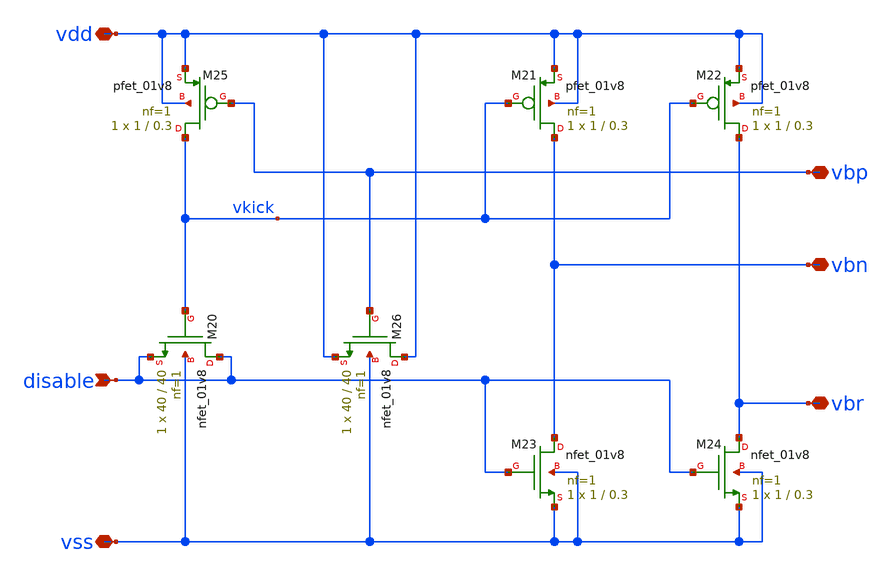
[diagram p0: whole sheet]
** sch_path: playground/ToBiasStartup.sch
**.subckt ToBiasStartup vss vdd vbp vbn vbr disable
*.iopin vss
*.iopin vdd
*.iopin vbp
*.iopin vbn
*.iopin vbr
*.ipin disable
XM24 vbr disable vss vss sky130_fd_pr__nfet_01v8 L=0.3 W=1 nf=1 ad='int((1 + 1)/2) * 1 / 1 * 0.29' as='int((1 + 2)/2) * 1 / 1 * 0.29'
+ pd='2*int((1 + 1)/2) * (1 / 1 + 0.29)' ps='2*int((1 + 2)/2) * (1 / 1 + 0.29)' nrd='0.29 / 1 ' nrs='0.29 / 1 '
+ sa=0 sb=0 sd=0 mult=1 m=1
XM22 vbr vkick vdd vdd sky130_fd_pr__pfet_01v8 L=0.3 W=1 nf=1 ad='int((nf+1)/2) * W/nf * 0.29' as='int((nf+2)/2) * W/nf * 0.29'
+ pd='2*int((nf+1)/2) * (W/nf + 0.29)' ps='2*int((nf+2)/2) * (W/nf + 0.29)' nrd='0.29 / W' nrs='0.29 / W'
+ sa=0 sb=0 sd=0 mult=1 m=1
XM25 vkick vbp vdd vdd sky130_fd_pr__pfet_01v8 L=0.3 W=1 nf=1 ad='int((nf+1)/2) * W/nf * 0.29' as='int((nf+2)/2) * W/nf * 0.29'
+ pd='2*int((nf+1)/2) * (W/nf + 0.29)' ps='2*int((nf+2)/2) * (W/nf + 0.29)' nrd='0.29 / W' nrs='0.29 / W'
+ sa=0 sb=0 sd=0 mult=1 m=1
XM23 vbn disable vss vss sky130_fd_pr__nfet_01v8 L=0.3 W=1 nf=1 ad='int((1 + 1)/2) * 1 / 1 * 0.29' as='int((1 + 2)/2) * 1 / 1 * 0.29'
+ pd='2*int((1 + 1)/2) * (1 / 1 + 0.29)' ps='2*int((1 + 2)/2) * (1 / 1 + 0.29)' nrd='0.29 / 1 ' nrs='0.29 / 1 '
+ sa=0 sb=0 sd=0 mult=1 m=1
XM21 vbn vkick vdd vdd sky130_fd_pr__pfet_01v8 L=0.3 W=1 nf=1 ad='int((nf+1)/2) * W/nf * 0.29' as='int((nf+2)/2) * W/nf * 0.29'
+ pd='2*int((nf+1)/2) * (W/nf + 0.29)' ps='2*int((nf+2)/2) * (W/nf + 0.29)' nrd='0.29 / W' nrs='0.29 / W'
+ sa=0 sb=0 sd=0 mult=1 m=1
XM20 disable vkick disable vss sky130_fd_pr__nfet_01v8 L=40 W=40 nf=1 ad='int((1 + 1)/2) * 40 / 1 * 0.29'
+ as='int((1 + 2)/2) * 40 / 1 * 0.29' pd='2*int((1 + 1)/2) * (40 / 1 + 0.29)' ps='2*int((1 + 2)/2) * (40 / 1 + 0.29)'
+ nrd='0.29 / 40 ' nrs='0.29 / 40 ' sa=0 sb=0 sd=0 mult=1 m=1
XM26 vdd vbp vdd vss sky130_fd_pr__nfet_01v8 L=40 W=40 nf=1 ad='int((1 + 1)/2) * 40 / 1 * 0.29' as='int((1 + 2)/2) * 40 / 1 * 0.29'
+ pd='2*int((1 + 1)/2) * (40 / 1 + 0.29)' ps='2*int((1 + 2)/2) * (40 / 1 + 0.29)' nrd='0.29 / 40 ' nrs='0.29 / 40 '
+ sa=0 sb=0 sd=0 mult=1 m=1
**.ends
.end
